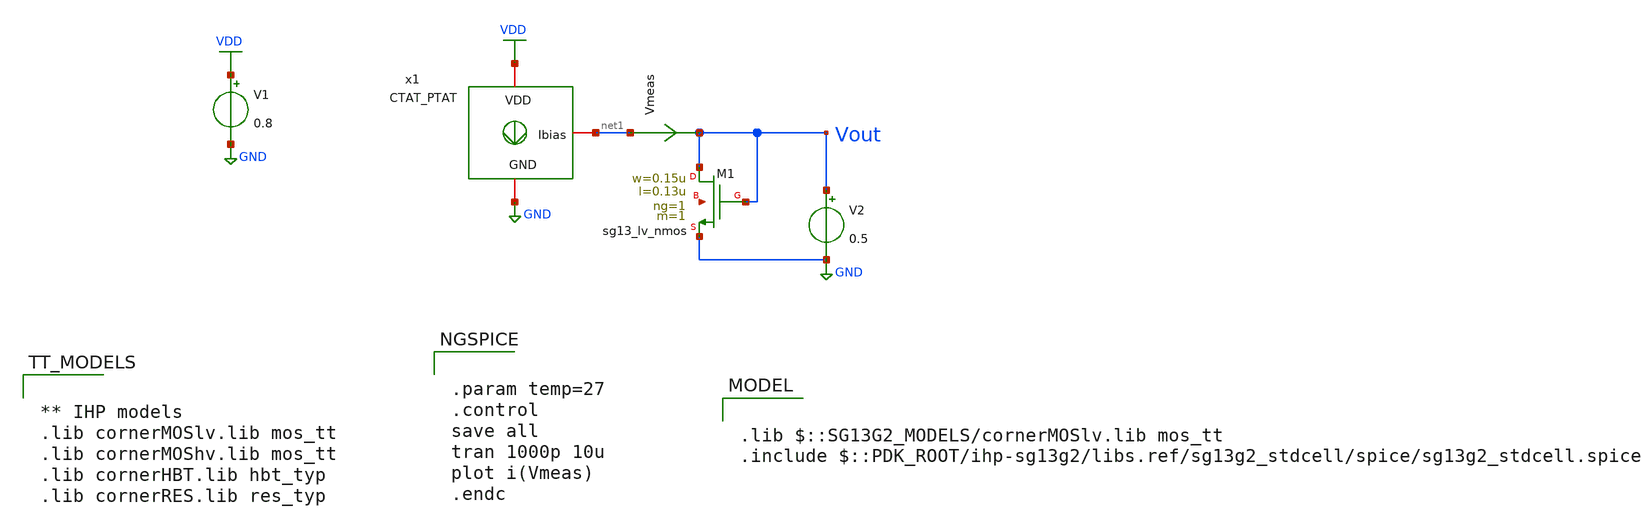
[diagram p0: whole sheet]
** sch_path: SSDOR_w_startup_1V_ihp/Ib_4u/CTAT_PTAT/tb_CTAT_PTAT.sch

.lib $::SG13G2_MODELS/cornerMOSlv.lib mos_tt
.include $::PDK_ROOT/ihp-sg13g2/libs.ref/sg13g2_stdcell/spice/sg13g2_stdcell.spice

**.subckt tb_CTAT_PTAT
V1 VDD GND 0.8
x1 VDD net1 GND CTAT_PTAT
V2 Vout GND 0.5
Vmeas net1 Vout 0
.save i(vmeas)
XM1 Vout Vout GND net2 sg13_lv_nmos w=0.15u l=0.13u ng=1 m=1 mm_ok=1
**** begin user architecture code


** IHP models
.lib cornerMOSlv.lib mos_tt
.lib cornerMOShv.lib mos_tt
.lib cornerHBT.lib hbt_typ
.lib cornerRES.lib res_typ




.param temp=27
.control
save all
tran 1000p 10u
plot i(Vmeas)
.endc


**** end user architecture code
**.ends
.GLOBAL VDD
.GLOBAL GND
.end
